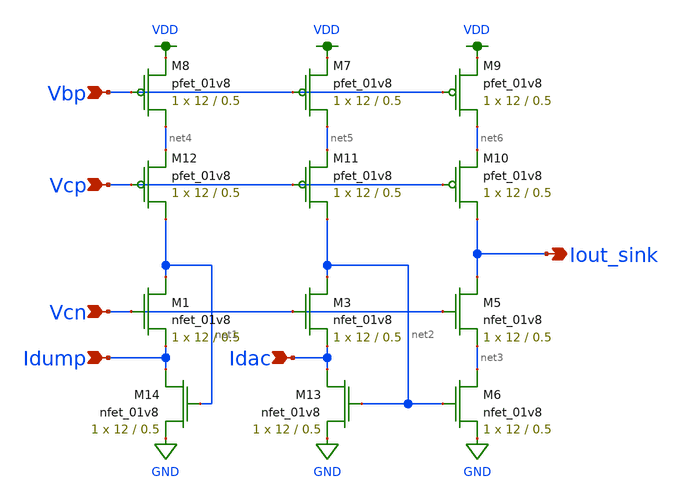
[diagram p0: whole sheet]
** sch_path: output_sink.sch
**.subckt output_sink Idump Idac Vcn Vcp Vbp Iout_sink
*.ipin Idump
*.ipin Idac
*.ipin Vcn
*.ipin Vcp
*.ipin Vbp
*.opin Iout_sink
XM1 net1 Vcn Idump GND sky130_fd_pr__nfet_01v8 L=0.5 W=12 nf=1 ad='int((nf+1)/2) * W/nf * 0.29' as='int((nf+2)/2) * W/nf * 0.29'
+ pd='2*int((nf+1)/2) * (W/nf + 0.29)' ps='2*int((nf+2)/2) * (W/nf + 0.29)' nrd='0.29 / W' nrs='0.29 / W'
+ sa=0 sb=0 sd=0 mult=1 m=1
XM8 net4 Vbp VDD VDD sky130_fd_pr__pfet_01v8 L=0.5 W=12 nf=1 ad='int((nf+1)/2) * W/nf * 0.29' as='int((nf+2)/2) * W/nf * 0.29'
+ pd='2*int((nf+1)/2) * (W/nf + 0.29)' ps='2*int((nf+2)/2) * (W/nf + 0.29)' nrd='0.29 / W' nrs='0.29 / W'
+ sa=0 sb=0 sd=0 mult=1 m=1
XM7 net5 Vbp VDD VDD sky130_fd_pr__pfet_01v8 L=0.5 W=12 nf=1 ad='int((nf+1)/2) * W/nf * 0.29' as='int((nf+2)/2) * W/nf * 0.29'
+ pd='2*int((nf+1)/2) * (W/nf + 0.29)' ps='2*int((nf+2)/2) * (W/nf + 0.29)' nrd='0.29 / W' nrs='0.29 / W'
+ sa=0 sb=0 sd=0 mult=1 m=1
XM9 net6 Vbp VDD VDD sky130_fd_pr__pfet_01v8 L=0.5 W=12 nf=1 ad='int((nf+1)/2) * W/nf * 0.29' as='int((nf+2)/2) * W/nf * 0.29'
+ pd='2*int((nf+1)/2) * (W/nf + 0.29)' ps='2*int((nf+2)/2) * (W/nf + 0.29)' nrd='0.29 / W' nrs='0.29 / W'
+ sa=0 sb=0 sd=0 mult=1 m=1
XM10 Iout_sink Vcp net6 VDD sky130_fd_pr__pfet_01v8 L=0.5 W=12 nf=1 ad='int((nf+1)/2) * W/nf * 0.29'
+ as='int((nf+2)/2) * W/nf * 0.29' pd='2*int((nf+1)/2) * (W/nf + 0.29)' ps='2*int((nf+2)/2) * (W/nf + 0.29)'
+ nrd='0.29 / W' nrs='0.29 / W' sa=0 sb=0 sd=0 mult=1 m=1
XM11 net2 Vcp net5 VDD sky130_fd_pr__pfet_01v8 L=0.5 W=12 nf=1 ad='int((nf+1)/2) * W/nf * 0.29' as='int((nf+2)/2) * W/nf * 0.29'
+ pd='2*int((nf+1)/2) * (W/nf + 0.29)' ps='2*int((nf+2)/2) * (W/nf + 0.29)' nrd='0.29 / W' nrs='0.29 / W'
+ sa=0 sb=0 sd=0 mult=1 m=1
XM12 net1 Vcp net4 VDD sky130_fd_pr__pfet_01v8 L=0.5 W=12 nf=1 ad='int((nf+1)/2) * W/nf * 0.29' as='int((nf+2)/2) * W/nf * 0.29'
+ pd='2*int((nf+1)/2) * (W/nf + 0.29)' ps='2*int((nf+2)/2) * (W/nf + 0.29)' nrd='0.29 / W' nrs='0.29 / W'
+ sa=0 sb=0 sd=0 mult=1 m=1
XM3 net2 Vcn Idac GND sky130_fd_pr__nfet_01v8 L=0.5 W=12 nf=1 ad='int((nf+1)/2) * W/nf * 0.29' as='int((nf+2)/2) * W/nf * 0.29'
+ pd='2*int((nf+1)/2) * (W/nf + 0.29)' ps='2*int((nf+2)/2) * (W/nf + 0.29)' nrd='0.29 / W' nrs='0.29 / W'
+ sa=0 sb=0 sd=0 mult=1 m=1
XM5 Iout_sink Vcn net3 GND sky130_fd_pr__nfet_01v8 L=0.5 W=12 nf=1 ad='int((nf+1)/2) * W/nf * 0.29' as='int((nf+2)/2) * W/nf * 0.29'
+ pd='2*int((nf+1)/2) * (W/nf + 0.29)' ps='2*int((nf+2)/2) * (W/nf + 0.29)' nrd='0.29 / W' nrs='0.29 / W'
+ sa=0 sb=0 sd=0 mult=1 m=1
XM6 net3 net2 GND GND sky130_fd_pr__nfet_01v8 L=0.5 W=12 nf=1 ad='int((nf+1)/2) * W/nf * 0.29' as='int((nf+2)/2) * W/nf * 0.29'
+ pd='2*int((nf+1)/2) * (W/nf + 0.29)' ps='2*int((nf+2)/2) * (W/nf + 0.29)' nrd='0.29 / W' nrs='0.29 / W'
+ sa=0 sb=0 sd=0 mult=1 m=1
XM13 Idac net2 GND GND sky130_fd_pr__nfet_01v8 L=0.5 W=12 nf=1 ad='int((nf+1)/2) * W/nf * 0.29' as='int((nf+2)/2) * W/nf * 0.29'
+ pd='2*int((nf+1)/2) * (W/nf + 0.29)' ps='2*int((nf+2)/2) * (W/nf + 0.29)' nrd='0.29 / W' nrs='0.29 / W'
+ sa=0 sb=0 sd=0 mult=1 m=1
XM14 Idump net1 GND GND sky130_fd_pr__nfet_01v8 L=0.5 W=12 nf=1 ad='int((nf+1)/2) * W/nf * 0.29' as='int((nf+2)/2) * W/nf * 0.29'
+ pd='2*int((nf+1)/2) * (W/nf + 0.29)' ps='2*int((nf+2)/2) * (W/nf + 0.29)' nrd='0.29 / W' nrs='0.29 / W'
+ sa=0 sb=0 sd=0 mult=1 m=1
**.ends
.GLOBAL GND
.GLOBAL VDD
.end
